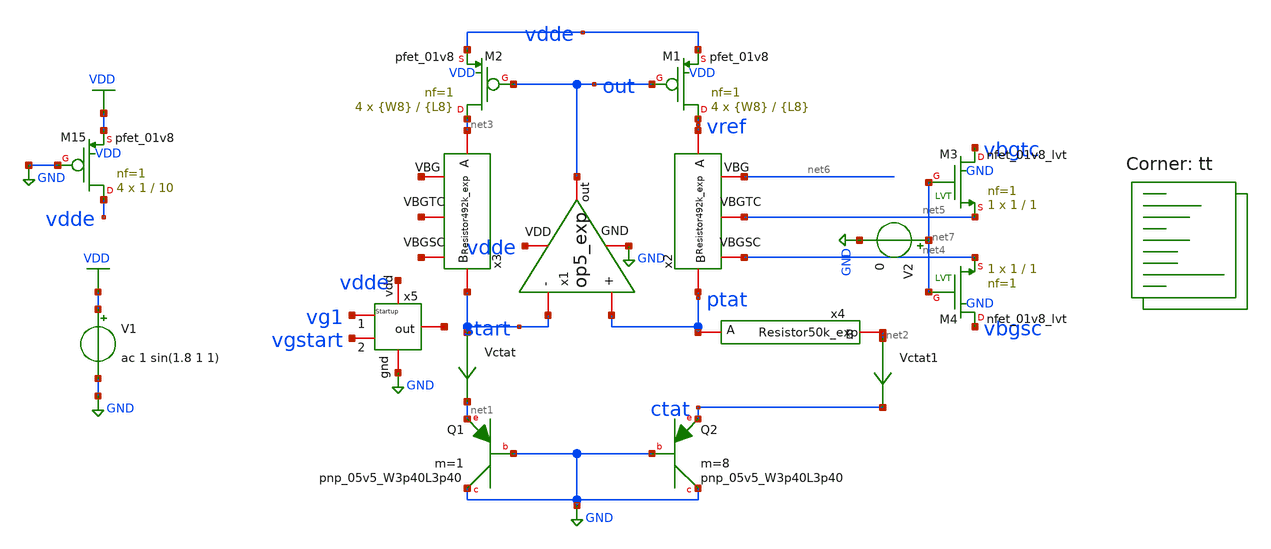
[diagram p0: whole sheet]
** sch_path: xschem/bgr_op5_exp.sch
**.subckt bgr_op5_exp
Vctat start net1 0
.save i(vctat)
V1 VDD GND ac 1 sin(1.8 1 1)
XM1 vref out vdde VDD sky130_fd_pr__pfet_01v8 L={L8} W={W8} nf=1 ad='int((nf+1)/2) * W/nf * 0.29' as='int((nf+2)/2) * W/nf * 0.29'
+ pd='2*int((nf+1)/2) * (W/nf + 0.29)' ps='2*int((nf+2)/2) * (W/nf + 0.29)' nrd='0.29 / W' nrs='0.29 / W'
+ sa=0 sb=0 sd=0 mult=4 m=4
XM2 net3 out vdde VDD sky130_fd_pr__pfet_01v8 L={L8} W={W8} nf=1 ad='int((nf+1)/2) * W/nf * 0.29' as='int((nf+2)/2) * W/nf * 0.29'
+ pd='2*int((nf+1)/2) * (W/nf + 0.29)' ps='2*int((nf+2)/2) * (W/nf + 0.29)' nrd='0.29 / W' nrs='0.29 / W'
+ sa=0 sb=0 sd=0 mult=4 m=4
XM15 vdde GND VDD VDD sky130_fd_pr__pfet_01v8 L=10 W=1 nf=1 ad='int((nf+1)/2) * W/nf * 0.29' as='int((nf+2)/2) * W/nf * 0.29'
+ pd='2*int((nf+1)/2) * (W/nf + 0.29)' ps='2*int((nf+2)/2) * (W/nf + 0.29)' nrd='0.29 / W' nrs='0.29 / W'
+ sa=0 sb=0 sd=0 mult=4 m=4
Vctat1 net2 ctat 0
.save i(vctat1)
x5 vdde vgstart vg1 net8 GND Startup
V2 net7 GND 0
XM3 vbgtc net7 net5 GND sky130_fd_pr__nfet_01v8_lvt L=1 W=1 nf=1 ad='int((nf+1)/2) * W/nf * 0.29' as='int((nf+2)/2) * W/nf * 0.29'
+ pd='2*int((nf+1)/2) * (W/nf + 0.29)' ps='2*int((nf+2)/2) * (W/nf + 0.29)' nrd='0.29 / W' nrs='0.29 / W'
+ sa=0 sb=0 sd=0 mult=1 m=1
XM4 vbgsc net7 net4 GND sky130_fd_pr__nfet_01v8_lvt L=1 W=1 nf=1 ad='int((nf+1)/2) * W/nf * 0.29' as='int((nf+2)/2) * W/nf * 0.29'
+ pd='2*int((nf+1)/2) * (W/nf + 0.29)' ps='2*int((nf+2)/2) * (W/nf + 0.29)' nrd='0.29 / W' nrs='0.29 / W'
+ sa=0 sb=0 sd=0 mult=1 m=1
x2 net6 vref ptat net5 net4 Resistor492k_exp
x3 net9 net3 start net10 net11 Resistor492k_exp
x4 net2 ptat Resistor50k_exp
x1 vdde out start ptat GND op5_exp
XQ2 GND GND ctat sky130_fd_pr__pnp_05v5_W3p40L3p40 m=8
XQ1 GND GND net1 sky130_fd_pr__pnp_05v5_W3p40L3p40 m=1
**** begin user architecture code


.param L8=10
.param W8=1
.param L10=1
.param W10=1
.param R=492k




.option savecurrents
.control
save all
op
remzerovec
write bgr_op5_exp.raw

set appendwrite
set wr_singlescale
set wr_vecnames
option numdgt=3

dc temp -40 85 1
remzerovec
write bgr_op5_exp.raw
*write VREFFS.raw vref
*plot (ptat-ctat)
*plot ctat
plot vref
*wrdata vref5.csv vref
*plot vbgsc vbgtc

********TC********
meas dc temp_avg_vref avg v(vref)
meas dc temp_vref_27 find v(vref) when temp-sweep=27
meas dc temp_pp_vref PP v(vref)
meas dc temp_vref_max max v(vref)
meas dc temp_max_vref when v(vref)='temp_vref_max'
meas dc temp_vref_min min v(vref)
meas dc temp_min_vref when v(vref)='temp_vref_min'
let vref_tc='((temp_pp_vref*1000000)/(125*temp_avg_vref))'
print vref_tc

******PSRR******
ac dec 1000 1 10Meg
write bgr_op5_exp.raw
*write PSRRFS.raw vdb(vref)
remzerovec
plot vdb(vref)
*wrdata PSRR5.csv vdb(vref)
meas ac psrr find vdb(vref) at=1k

****Power****
tran 10ms 500ms
write bgr_op5_exp.raw
set altshow
show >> bgr_op5_exp.lis
remzerovec
meas tran ave_v avg vdd
meas tran ave_i avg i(v1)
let ave_power='ave_v*(-ave_i)
plot vdd vref
plot vg1 vgstart start
*plot -i(v1)
print ave_power

*******LS******
dc v1 0 3.5 0.1
write bgr_op5_exp.raw
remzerovec
plot vdd vref
meas dc vbg_27 find v(vref) at=1.8
meas dc vbgsc_27 find v(vbgsc) at=1.8
meas dc vbgtc_27 find v(vbgtc) at=1.8
meas dc vref_max max v(vref) from=1.62 to=1.98
meas dc vref_min min v(vref) from=1.62 to=1.98
let ls='(vref_max-vref_min)/(1.98-1.62)'
print ls

.endc


.lib $::SKYWATER_MODELS/sky130.lib.spice tt
**** end user architecture code
**.ends

* expanding   symbol:  Startup.sym # of pins=5
** sym_path: xschem/Startup.sym
** sch_path: xschem/Startup.sch
.subckt Startup vdd 2 1 out gnd
*.iopin vdd
*.iopin gnd
*.iopin out
*.iopin 1
*.iopin 2
XM1 1 out gnd GND sky130_fd_pr__nfet_01v8 L=1 W=1 nf=1 ad='int((nf+1)/2) * W/nf * 0.29' as='int((nf+2)/2)
+ * W/nf * 0.29' pd='2*int((nf+1)/2) * (W/nf + 0.29)' ps='2*int((nf+2)/2) * (W/nf + 0.29)' nrd='0.29 /
+ W' nrs='0.29 / W' sa=0 sb=0 sd=0 mult=4 m=4
XM2 2 1 vdd VDD sky130_fd_pr__pfet_01v8 L=10 W=1 nf=1 ad='int((nf+1)/2) * W/nf * 0.29' as='int((nf+2)/2)
+ * W/nf * 0.29' pd='2*int((nf+1)/2) * (W/nf + 0.29)' ps='2*int((nf+2)/2) * (W/nf + 0.29)' nrd='0.29 /
+ W' nrs='0.29 / W' sa=0 sb=0 sd=0 mult=1 m=1
XM3 1 1 vdd VDD sky130_fd_pr__pfet_01v8 L=10 W=1 nf=1 ad='int((nf+1)/2) * W/nf * 0.29' as='int((nf+2)/2)
+ * W/nf * 0.29' pd='2*int((nf+1)/2) * (W/nf + 0.29)' ps='2*int((nf+2)/2) * (W/nf + 0.29)' nrd='0.29 /
+ W' nrs='0.29 / W' sa=0 sb=0 sd=0 mult=1 m=1
XM4 out 2 vdd VDD sky130_fd_pr__pfet_01v8 L=10 W=1 nf=1 ad='int((nf+1)/2) * W/nf * 0.29' as='int((nf+2)/2)
+ * W/nf * 0.29' pd='2*int((nf+1)/2) * (W/nf + 0.29)' ps='2*int((nf+2)/2) * (W/nf + 0.29)' nrd='0.29 /
+ W' nrs='0.29 / W' sa=0 sb=0 sd=0 mult=1 m=1
x1 gnd 2 ResistorStart
.ends


* expanding   symbol:  Resistor492k_exp.sym # of pins=5
** sym_path: xschem/Resistor492k_exp.sym
** sch_path: xschem/Resistor492k_exp.sch
.subckt Resistor492k_exp VBG A B VBGTC VBGSC
*.iopin A
*.iopin VBGTC
*.iopin B
*.iopin VBGSC
*.iopin VBG
XR1 net1 A GND sky130_fd_pr__res_high_po_0p35 L={L} mult=1 m=1
XR2 net2 net1 GND sky130_fd_pr__res_high_po_0p35 L={L} mult=1 m=1
XR3 VBG net2 GND sky130_fd_pr__res_high_po_0p35 L={L} mult=1 m=1
XR4 net3 VBG GND sky130_fd_pr__res_high_po_0p35 L={L} mult=1 m=1
XR5 net4 net3 GND sky130_fd_pr__res_high_po_0p35 L={L} mult=1 m=1
**** begin user architecture code


.param L=17


**** end user architecture code
XR6 net5 net6 GND sky130_fd_pr__res_high_po_0p35 L={L} mult=1 m=1
XR7 VBGSC net5 GND sky130_fd_pr__res_high_po_0p35 L={L} mult=1 m=1
XR8 VBGTC VBGSC GND sky130_fd_pr__res_high_po_0p35 L={L} mult=1 m=1
XR9 net7 VBGTC GND sky130_fd_pr__res_high_po_0p35 L={L} mult=1 m=1
XR10 net4 net7 GND sky130_fd_pr__res_high_po_0p35 L={L} mult=1 m=1
XR11 net8 net6 GND sky130_fd_pr__res_high_po_0p35 L={L} mult=1 m=1
XR12 net9 net8 GND sky130_fd_pr__res_high_po_0p35 L={L} mult=1 m=1
XR13 net11 net9 GND sky130_fd_pr__res_high_po_0p35 L={L} mult=1 m=1
XR14 net10 net11 GND sky130_fd_pr__res_high_po_0p35 L={L} mult=1 m=1
XR15 net12 net10 GND sky130_fd_pr__res_high_po_0p35 L={L} mult=1 m=1
XR20 net12 net13 GND sky130_fd_pr__res_high_po_0p35 L={L} mult=1 m=1
XR16 net13 net14 GND sky130_fd_pr__res_high_po_0p35 L={L} mult=1 m=1
XR17 net14 net15 GND sky130_fd_pr__res_high_po_0p35 L={L} mult=1 m=1
XR18 net15 net16 GND sky130_fd_pr__res_high_po_0p35 L={L} mult=1 m=1
XR19 net16 net17 GND sky130_fd_pr__res_high_po_0p35 L={L} mult=1 m=1
XR21 B net18 GND sky130_fd_pr__res_high_po_0p35 L={L} mult=1 m=1
XR22 net18 net17 GND sky130_fd_pr__res_high_po_0p35 L={L} mult=1 m=1
.ends


* expanding   symbol:  Resistor50k_exp.sym # of pins=2
** sym_path: xschem/Resistor50k_exp.sym
** sch_path: xschem/Resistor50k_exp.sch
.subckt Resistor50k_exp B A
*.iopin A
*.iopin B
XR2 net2 net1 GND sky130_fd_pr__res_high_po_0p35 L={L} mult=1 m=1
**** begin user architecture code


.param L=17
.param La=17
.param L1=1
.param W1=15


**** end user architecture code
XR3 A net2 GND sky130_fd_pr__res_high_po_0p35 L={L} mult=1 m=1
XR1 net1 net3 GND sky130_fd_pr__res_high_po_0p35 L={La} mult=2 m=2
XR4 net3 net4 GND sky130_fd_pr__res_high_po_0p35 L={La} mult=4 m=4
XR5 net4 net5 GND sky130_fd_pr__res_high_po_0p35 L={La} mult=8 m=8
XR6 net5 B GND sky130_fd_pr__res_high_po_0p35 L={La} mult=16 m=16
V1 net6 GND 1.8
XM4 net1 net6 net3 GND sky130_fd_pr__nfet_01v8_lvt L={L1} W={W1} nf=1 ad='int((nf+1)/2) * W/nf * 0.29' as='int((nf+2)/2)
+ * W/nf * 0.29' pd='2*int((nf+1)/2) * (W/nf + 0.29)' ps='2*int((nf+2)/2) * (W/nf + 0.29)' nrd='0.29 /
+ W' nrs='0.29 / W' sa=0 sb=0 sd=0 mult=1 m=1
XM1 net3 GND net4 GND sky130_fd_pr__nfet_01v8_lvt L={L1} W={W1} nf=1 ad='int((nf+1)/2) * W/nf * 0.29' as='int((nf+2)/2)
+ * W/nf * 0.29' pd='2*int((nf+1)/2) * (W/nf + 0.29)' ps='2*int((nf+2)/2) * (W/nf + 0.29)' nrd='0.29 /
+ W' nrs='0.29 / W' sa=0 sb=0 sd=0 mult=1 m=1
XM2 net4 GND net5 GND sky130_fd_pr__nfet_01v8_lvt L={L1} W={W1} nf=1 ad='int((nf+1)/2) * W/nf * 0.29' as='int((nf+2)/2)
+ * W/nf * 0.29' pd='2*int((nf+1)/2) * (W/nf + 0.29)' ps='2*int((nf+2)/2) * (W/nf + 0.29)' nrd='0.29 /
+ W' nrs='0.29 / W' sa=0 sb=0 sd=0 mult=1 m=1
XM3 net5 GND B GND sky130_fd_pr__nfet_01v8_lvt L={L1} W={W1} nf=1 ad='int((nf+1)/2) * W/nf * 0.29' as='int((nf+2)/2)
+ * W/nf * 0.29' pd='2*int((nf+1)/2) * (W/nf + 0.29)' ps='2*int((nf+2)/2) * (W/nf + 0.29)' nrd='0.29 /
+ W' nrs='0.29 / W' sa=0 sb=0 sd=0 mult=1 m=1
.ends


* expanding   symbol:  op5_exp.sym # of pins=5
** sym_path: xschem/op5_exp.sym
** sch_path: xschem/op5_exp.sch
.subckt op5_exp VDD out - + GND
*.iopin GND
*.iopin -
*.iopin +
*.iopin VDD
*.iopin out
XM8 net1 net2 VDD VDD sky130_fd_pr__pfet_01v8 L={L7} W={W7} nf=1 ad='int((nf+1)/2) * W/nf * 0.29' as='int((nf+2)/2)
+ * W/nf * 0.29' pd='2*int((nf+1)/2) * (W/nf + 0.29)' ps='2*int((nf+2)/2) * (W/nf + 0.29)' nrd='0.29 /
+ W' nrs='0.29 / W' sa=0 sb=0 sd=0 mult=4 m=4
XM9 net2 net2 VDD VDD sky130_fd_pr__pfet_01v8 L={L7} W={W7} nf=1 ad='int((nf+1)/2) * W/nf * 0.29' as='int((nf+2)/2)
+ * W/nf * 0.29' pd='2*int((nf+1)/2) * (W/nf + 0.29)' ps='2*int((nf+2)/2) * (W/nf + 0.29)' nrd='0.29 /
+ W' nrs='0.29 / W' sa=0 sb=0 sd=0 mult=4 m=4
XM5 net3 bias GND GND sky130_fd_pr__nfet_01v8 L={L6} W={W6} nf=1 ad='int((nf+1)/2) * W/nf * 0.29' as='int((nf+2)/2)
+ * W/nf * 0.29' pd='2*int((nf+1)/2) * (W/nf + 0.29)' ps='2*int((nf+2)/2) * (W/nf + 0.29)' nrd='0.29 /
+ W' nrs='0.29 / W' sa=0 sb=0 sd=0 mult=2 m=2
XM10 out net1 VDD VDD sky130_fd_pr__pfet_01v8 L={L2} W={W2} nf=1 ad='int((nf+1)/2) * W/nf * 0.29' as='int((nf+2)/2)
+ * W/nf * 0.29' pd='2*int((nf+1)/2) * (W/nf + 0.29)' ps='2*int((nf+2)/2) * (W/nf + 0.29)' nrd='0.29 /
+ W' nrs='0.29 / W' sa=0 sb=0 sd=0 mult=4 m=4
**** begin user architecture code


**************
*PMOS cms
.param L1=20
.param W1=1
**************
*PMOS current differential
.param L7=10
.param W7=1

**************
*differential Pair
.param L4=10
.param W4=0.6

**************
*NMOS current control
.param L6=20
.param W6=1

**************
*Second Stage
.param L2=7
.param W2=1


**** end user architecture code
XM11 out bias GND GND sky130_fd_pr__nfet_01v8 L={L6} W={W6} nf=1 ad='int((nf+1)/2) * W/nf * 0.29' as='int((nf+2)/2)
+ * W/nf * 0.29' pd='2*int((nf+1)/2) * (W/nf + 0.29)' ps='2*int((nf+2)/2) * (W/nf + 0.29)' nrd='0.29 /
+ W' nrs='0.29 / W' sa=0 sb=0 sd=0 mult=2 m=2
XM3 net1 + net3 GND sky130_fd_pr__nfet_01v8 L={L4} W={W4} nf=1 ad='int((nf+1)/2) * W/nf * 0.29' as='int((nf+2)/2)
+ * W/nf * 0.29' pd='2*int((nf+1)/2) * (W/nf + 0.29)' ps='2*int((nf+2)/2) * (W/nf + 0.29)' nrd='0.29 /
+ W' nrs='0.29 / W' sa=0 sb=0 sd=0 mult=4 m=4
XM1 bias net6 VDD VDD sky130_fd_pr__pfet_01v8 L={L1} W={W1} nf=1 ad='int((nf+1)/2) * W/nf * 0.29' as='int((nf+2)/2)
+ * W/nf * 0.29' pd='2*int((nf+1)/2) * (W/nf + 0.29)' ps='2*int((nf+2)/2) * (W/nf + 0.29)' nrd='0.29 /
+ W' nrs='0.29 / W' sa=0 sb=0 sd=0 mult=2 m=2
XM2 net6 net6 VDD VDD sky130_fd_pr__pfet_01v8 L={L1} W={W1} nf=1 ad='int((nf+1)/2) * W/nf * 0.29' as='int((nf+2)/2)
+ * W/nf * 0.29' pd='2*int((nf+1)/2) * (W/nf + 0.29)' ps='2*int((nf+2)/2) * (W/nf + 0.29)' nrd='0.29 /
+ W' nrs='0.29 / W' sa=0 sb=0 sd=0 mult=2 m=2
XM6 net6 bias net7 GND sky130_fd_pr__nfet_01v8 L={L6} W={W6} nf=1 ad='int((nf+1)/2) * W/nf * 0.29' as='int((nf+2)/2)
+ * W/nf * 0.29' pd='2*int((nf+1)/2) * (W/nf + 0.29)' ps='2*int((nf+2)/2) * (W/nf + 0.29)' nrd='0.29 /
+ W' nrs='0.29 / W' sa=0 sb=0 sd=0 mult=2 m=2
XM7 bias bias GND GND sky130_fd_pr__nfet_01v8 L={L6} W={W6} nf=1 ad='int((nf+1)/2) * W/nf * 0.29' as='int((nf+2)/2)
+ * W/nf * 0.29' pd='2*int((nf+1)/2) * (W/nf + 0.29)' ps='2*int((nf+2)/2) * (W/nf + 0.29)' nrd='0.29 /
+ W' nrs='0.29 / W' sa=0 sb=0 sd=0 mult=2 m=2
XR4 net7 GND GND sky130_fd_pr__res_high_po_0p35 L=3 mult=8 m=8
XM4 net2 - net3 GND sky130_fd_pr__nfet_01v8 L={L4} W={W4} nf=1 ad='int((nf+1)/2) * W/nf * 0.29' as='int((nf+2)/2)
+ * W/nf * 0.29' pd='2*int((nf+1)/2) * (W/nf + 0.29)' ps='2*int((nf+2)/2) * (W/nf + 0.29)' nrd='0.29 /
+ W' nrs='0.29 / W' sa=0 sb=0 sd=0 mult=4 m=4
XR1 net1 net4 GND sky130_fd_pr__res_high_po_0p35 L=3 mult=4 m=4
XR2 net4 net5 GND sky130_fd_pr__res_high_po_0p35 L=3 mult=4 m=4
XC1 out net5 sky130_fd_pr__cap_mim_m3_1 W=17 L=17 MF=4 m=4
.ends


* expanding   symbol:  ResistorStart.sym # of pins=2
** sym_path: xschem/ResistorStart.sym
** sch_path: xschem/ResistorStart.sch
.subckt ResistorStart B A
*.iopin A
*.iopin B
XR1 net1 A GND sky130_fd_pr__res_high_po_0p35 L=17 mult=1 m=1
XR2 net2 net1 GND sky130_fd_pr__res_high_po_0p35 L={L} mult=1 m=1
XR3 net4 net2 GND sky130_fd_pr__res_high_po_0p35 L={L} mult=1 m=1
XR4 net3 net4 GND sky130_fd_pr__res_high_po_0p35 L={L} mult=1 m=1
XR5 net5 net3 GND sky130_fd_pr__res_high_po_0p35 L={L} mult=1 m=1
**** begin user architecture code


.param L=17


**** end user architecture code
XR6 net6 net7 GND sky130_fd_pr__res_high_po_0p35 L={L} mult=1 m=1
XR7 net8 net6 GND sky130_fd_pr__res_high_po_0p35 L={L} mult=1 m=1
XR8 net10 net8 GND sky130_fd_pr__res_high_po_0p35 L={L} mult=1 m=1
XR9 net9 net10 GND sky130_fd_pr__res_high_po_0p35 L={L} mult=1 m=1
XR10 net5 net9 GND sky130_fd_pr__res_high_po_0p35 L={L} mult=1 m=1
XR11 net11 net7 GND sky130_fd_pr__res_high_po_0p35 L={L} mult=1 m=1
XR12 net12 net11 GND sky130_fd_pr__res_high_po_0p35 L={L} mult=1 m=1
XR13 net14 net12 GND sky130_fd_pr__res_high_po_0p35 L={L} mult=1 m=1
XR14 net13 net14 GND sky130_fd_pr__res_high_po_0p35 L={L} mult=1 m=1
XR15 net15 net13 GND sky130_fd_pr__res_high_po_0p35 L={L} mult=1 m=1
XR16 net16 net17 GND sky130_fd_pr__res_high_po_0p35 L={L} mult=1 m=1
XR17 net18 net16 GND sky130_fd_pr__res_high_po_0p35 L={L} mult=1 m=1
XR18 net20 net18 GND sky130_fd_pr__res_high_po_0p35 L={L} mult=1 m=1
XR19 net19 net20 GND sky130_fd_pr__res_high_po_0p35 L={L} mult=1 m=1
XR20 net15 net19 GND sky130_fd_pr__res_high_po_0p35 L={L} mult=1 m=1
XR21 net21 net17 GND sky130_fd_pr__res_high_po_0p35 L={L} mult=1 m=1
XR22 net22 net21 GND sky130_fd_pr__res_high_po_0p35 L={L} mult=1 m=1
XR23 net23 net22 GND sky130_fd_pr__res_high_po_0p35 L={L} mult=1 m=1
XR24 net24 net23 GND sky130_fd_pr__res_high_po_0p35 L={L} mult=1 m=1
XR25 net25 net24 GND sky130_fd_pr__res_high_po_0p35 L={L} mult=1 m=1
XR26 net26 B GND sky130_fd_pr__res_high_po_0p35 L={L} mult=1 m=1
XR27 net27 net26 GND sky130_fd_pr__res_high_po_0p35 L={L} mult=1 m=1
XR28 net28 net27 GND sky130_fd_pr__res_high_po_0p35 L={L} mult=1 m=1
XR29 net29 net28 GND sky130_fd_pr__res_high_po_0p35 L={L} mult=1 m=1
XR30 net25 net29 GND sky130_fd_pr__res_high_po_0p35 L={L} mult=1 m=1
.ends

.GLOBAL GND
.GLOBAL VDD
.end
